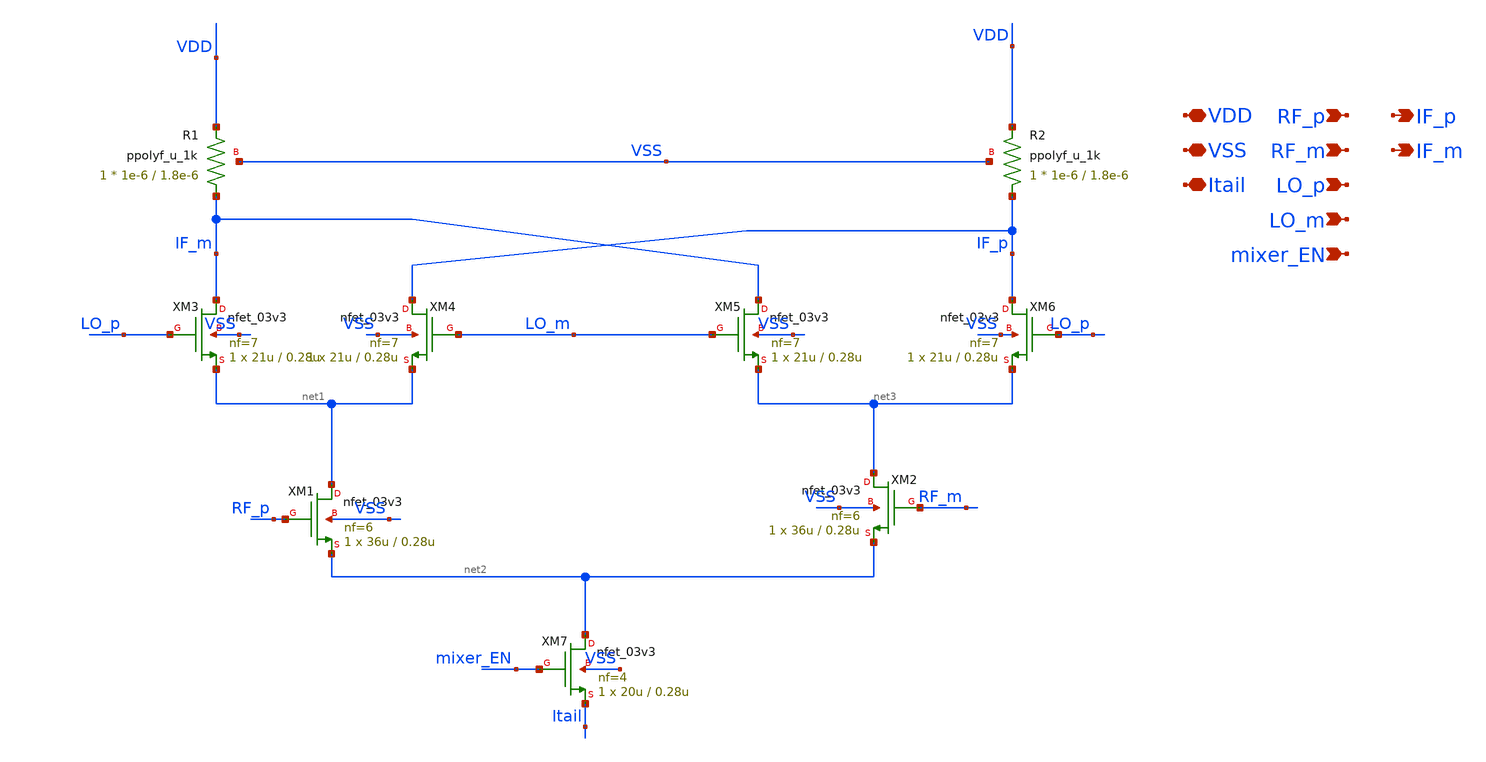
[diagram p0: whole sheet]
** sch_path: designs/mixer/schematic/mixer.sch
**.subckt mixer VDD LO_p LO_m Itail IF_m IF_p VSS RF_p RF_m mixer_EN
*.iopin VDD
*.ipin LO_p
*.ipin LO_m
*.iopin Itail
*.opin IF_m
*.opin IF_p
*.iopin VSS
*.ipin RF_p
*.ipin RF_m
*.ipin mixer_EN
XM1 net1 RF_p net2 VSS nfet_03v3 L=0.28u W=36u nf=6 ad='int((nf+1)/2) * W/nf * 0.18u' as='int((nf+2)/2) * W/nf * 0.18u'
+ pd='2*int((nf+1)/2) * (W/nf + 0.18u)' ps='2*int((nf+2)/2) * (W/nf + 0.18u)' nrd='0.18u / W' nrs='0.18u / W'
+ sa=0 sb=0 sd=0 m=1
XM2 net3 RF_m net2 VSS nfet_03v3 L=0.28u W=36u nf=6 ad='int((nf+1)/2) * W/nf * 0.18u' as='int((nf+2)/2) * W/nf * 0.18u'
+ pd='2*int((nf+1)/2) * (W/nf + 0.18u)' ps='2*int((nf+2)/2) * (W/nf + 0.18u)' nrd='0.18u / W' nrs='0.18u / W'
+ sa=0 sb=0 sd=0 m=1
XM3 IF_m LO_p net1 VSS nfet_03v3 L=0.28u W=21u nf=7 ad='int((nf+1)/2) * W/nf * 0.18u' as='int((nf+2)/2) * W/nf * 0.18u'
+ pd='2*int((nf+1)/2) * (W/nf + 0.18u)' ps='2*int((nf+2)/2) * (W/nf + 0.18u)' nrd='0.18u / W' nrs='0.18u / W'
+ sa=0 sb=0 sd=0 m=1
XM4 IF_p LO_m net1 VSS nfet_03v3 L=0.28u W=21u nf=7 ad='int((nf+1)/2) * W/nf * 0.18u' as='int((nf+2)/2) * W/nf * 0.18u'
+ pd='2*int((nf+1)/2) * (W/nf + 0.18u)' ps='2*int((nf+2)/2) * (W/nf + 0.18u)' nrd='0.18u / W' nrs='0.18u / W'
+ sa=0 sb=0 sd=0 m=1
XM5 IF_m LO_m net3 VSS nfet_03v3 L=0.28u W=21u nf=7 ad='int((nf+1)/2) * W/nf * 0.18u' as='int((nf+2)/2) * W/nf * 0.18u'
+ pd='2*int((nf+1)/2) * (W/nf + 0.18u)' ps='2*int((nf+2)/2) * (W/nf + 0.18u)' nrd='0.18u / W' nrs='0.18u / W'
+ sa=0 sb=0 sd=0 m=1
XM6 IF_p LO_p net3 VSS nfet_03v3 L=0.28u W=21u nf=7 ad='int((nf+1)/2) * W/nf * 0.18u' as='int((nf+2)/2) * W/nf * 0.18u'
+ pd='2*int((nf+1)/2) * (W/nf + 0.18u)' ps='2*int((nf+2)/2) * (W/nf + 0.18u)' nrd='0.18u / W' nrs='0.18u / W'
+ sa=0 sb=0 sd=0 m=1
XM7 net2 mixer_EN Itail VSS nfet_03v3 L=0.28u W=20u nf=4 ad='int((nf+1)/2) * W/nf * 0.18u' as='int((nf+2)/2) * W/nf * 0.18u'
+ pd='2*int((nf+1)/2) * (W/nf + 0.18u)' ps='2*int((nf+2)/2) * (W/nf + 0.18u)' nrd='0.18u / W' nrs='0.18u / W'
+ sa=0 sb=0 sd=0 m=1
XR1 IF_m VDD VSS ppolyf_u_1k r_width=1e-6 r_length=1.8e-6 m=1
XR2 IF_p VDD VSS ppolyf_u_1k r_width=1e-6 r_length=1.8e-6 m=1
**.ends
.end
